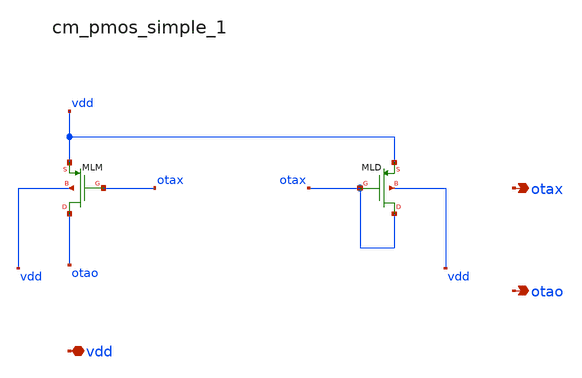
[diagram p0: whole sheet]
** sch_path: analog-db/raw/ldo_009_fer_5t_pass/hier/blocks/cm_pmos_simple_1.sch
**.subckt cm_pmos_simple_1 vdd otax otao
*.iopin vdd
*.opin otax
*.opin otao
XMLD otax otax vdd vdd sg13_lv_pmos w=x_dut_xmld_w l=x_dut_xmld_l ng=1 m=x_dut_xmld_m
XMLM otao otax vdd vdd sg13_lv_pmos w=x_dut_xmlm_w l=x_dut_xmlm_l ng=1 m=x_dut_xmlm_m
**.ends
.end
